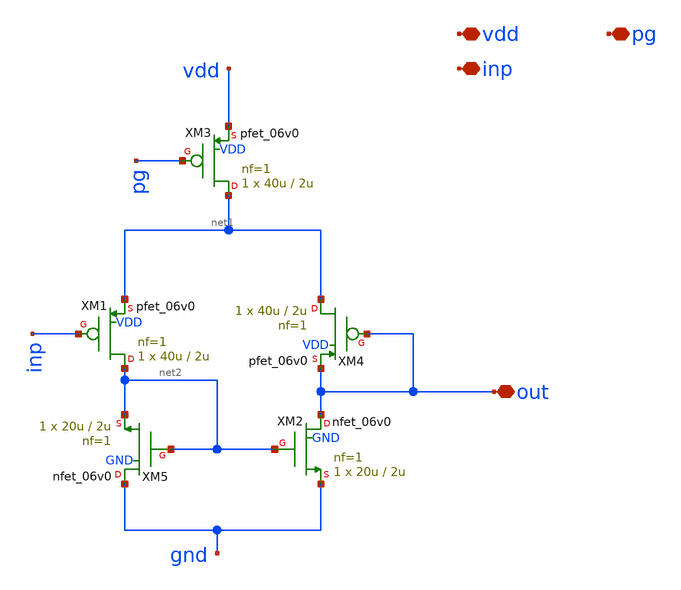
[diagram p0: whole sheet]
** sch_path: Schematics #2/xschem/ota5.sch
**.subckt ota5 inp out vdd pg
*.iopin inp
*.iopin out
*.iopin vdd
*.iopin pg
XM1 net2 inp net1 VDD pfet_06v0 L=2u W=40u nf=1 ad='int((nf+1)/2) * W/nf * 0.18u' as='int((nf+2)/2) * W/nf * 0.18u'
+ pd='2*int((nf+1)/2) * (W/nf + 0.18u)' ps='2*int((nf+2)/2) * (W/nf + 0.18u)' nrd='0.18u / W' nrs='0.18u / W'
+ sa=0 sb=0 sd=0 m=1 par=1
XM2 out net2 gnd GND nfet_06v0 L=2u W=20u nf=1 ad='int((nf+1)/2) * W/nf * 0.18u' as='int((nf+2)/2) * W/nf * 0.18u'
+ pd='2*int((nf+1)/2) * (W/nf + 0.18u)' ps='2*int((nf+2)/2) * (W/nf + 0.18u)' nrd='0.18u / W' nrs='0.18u / W'
+ sa=0 sb=0 sd=0 m=1 par=1
XM3 net1 pg vdd VDD pfet_06v0 L=2u W=40u nf=1 ad='int((nf+1)/2) * W/nf * 0.18u' as='int((nf+2)/2) * W/nf * 0.18u'
+ pd='2*int((nf+1)/2) * (W/nf + 0.18u)' ps='2*int((nf+2)/2) * (W/nf + 0.18u)' nrd='0.18u / W' nrs='0.18u / W'
+ sa=0 sb=0 sd=0 m=1 par=1
XM4 net1 out out VDD pfet_06v0 L=2u W=40u nf=1 ad='int((nf+1)/2) * W/nf * 0.18u' as='int((nf+2)/2) * W/nf * 0.18u'
+ pd='2*int((nf+1)/2) * (W/nf + 0.18u)' ps='2*int((nf+2)/2) * (W/nf + 0.18u)' nrd='0.18u / W' nrs='0.18u / W'
+ sa=0 sb=0 sd=0 m=1 par=1
XM5 gnd net2 net2 GND nfet_06v0 L=2u W=20u nf=1 ad='int((nf+1)/2) * W/nf * 0.18u' as='int((nf+2)/2) * W/nf * 0.18u'
+ pd='2*int((nf+1)/2) * (W/nf + 0.18u)' ps='2*int((nf+2)/2) * (W/nf + 0.18u)' nrd='0.18u / W' nrs='0.18u / W'
+ sa=0 sb=0 sd=0 m=1 par=1
**.ends
.end
